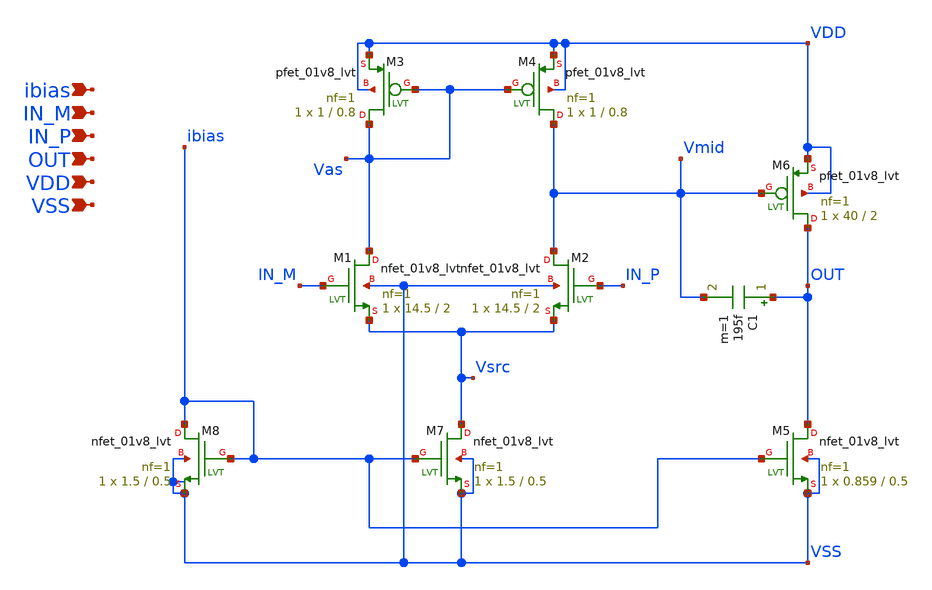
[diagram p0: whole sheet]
** sch_path: xchem/OTA3_kh.sch
**.subckt OTA3_kh IN_M IN_P OUT ibias VDD VSS
*.ipin IN_M
*.ipin IN_P
*.ipin OUT
*.ipin ibias
*.ipin VDD
*.ipin VSS
XM1 Vas IN_M Vsrc VSS sky130_fd_pr__nfet_01v8_lvt L=2 W=14.5 nf=1 ad='int((nf+1)/2) * W/nf * 0.29' as='int((nf+2)/2) * W/nf * 0.29'
+ pd='2*int((nf+1)/2) * (W/nf + 0.29)' ps='2*int((nf+2)/2) * (W/nf + 0.29)' nrd='0.29 / W' nrs='0.29 / W'
+ sa=0 sb=0 sd=0 mult=1 m=1
XM2 Vmid IN_P Vsrc VSS sky130_fd_pr__nfet_01v8_lvt L=2 W=14.5 nf=1 ad='int((nf+1)/2) * W/nf * 0.29' as='int((nf+2)/2) * W/nf * 0.29'
+ pd='2*int((nf+1)/2) * (W/nf + 0.29)' ps='2*int((nf+2)/2) * (W/nf + 0.29)' nrd='0.29 / W' nrs='0.29 / W'
+ sa=0 sb=0 sd=0 mult=1 m=1
XM3 Vas Vas VDD VDD sky130_fd_pr__pfet_01v8_lvt L=0.8 W=1 nf=1 ad='int((nf+1)/2) * W/nf * 0.29' as='int((nf+2)/2) * W/nf * 0.29'
+ pd='2*int((nf+1)/2) * (W/nf + 0.29)' ps='2*int((nf+2)/2) * (W/nf + 0.29)' nrd='0.29 / W' nrs='0.29 / W'
+ sa=0 sb=0 sd=0 mult=1 m=1
XM4 Vmid Vas VDD VDD sky130_fd_pr__pfet_01v8_lvt L=0.8 W=1 nf=1 ad='int((nf+1)/2) * W/nf * 0.29' as='int((nf+2)/2) * W/nf * 0.29'
+ pd='2*int((nf+1)/2) * (W/nf + 0.29)' ps='2*int((nf+2)/2) * (W/nf + 0.29)' nrd='0.29 / W' nrs='0.29 / W'
+ sa=0 sb=0 sd=0 mult=1 m=1
XM6 OUT Vmid VDD VDD sky130_fd_pr__pfet_01v8_lvt L=2 W=40 nf=1 ad='int((nf+1)/2) * W/nf * 0.29' as='int((nf+2)/2) * W/nf * 0.29'
+ pd='2*int((nf+1)/2) * (W/nf + 0.29)' ps='2*int((nf+2)/2) * (W/nf + 0.29)' nrd='0.29 / W' nrs='0.29 / W'
+ sa=0 sb=0 sd=0 mult=1 m=1
XM5 OUT ibias VSS VSS sky130_fd_pr__nfet_01v8_lvt L=0.5 W=0.859 nf=1 ad='int((nf+1)/2) * W/nf * 0.29'
+ as='int((nf+2)/2) * W/nf * 0.29' pd='2*int((nf+1)/2) * (W/nf + 0.29)' ps='2*int((nf+2)/2) * (W/nf + 0.29)'
+ nrd='0.29 / W' nrs='0.29 / W' sa=0 sb=0 sd=0 mult=1 m=1
XM7 Vsrc ibias VSS VSS sky130_fd_pr__nfet_01v8_lvt L=0.5 W=1.5 nf=1 ad='int((nf+1)/2) * W/nf * 0.29'
+ as='int((nf+2)/2) * W/nf * 0.29' pd='2*int((nf+1)/2) * (W/nf + 0.29)' ps='2*int((nf+2)/2) * (W/nf + 0.29)'
+ nrd='0.29 / W' nrs='0.29 / W' sa=0 sb=0 sd=0 mult=1 m=1
XM8 ibias ibias VSS VSS sky130_fd_pr__nfet_01v8_lvt L=0.5 W=1.5 nf=1 ad='int((nf+1)/2) * W/nf * 0.29'
+ as='int((nf+2)/2) * W/nf * 0.29' pd='2*int((nf+1)/2) * (W/nf + 0.29)' ps='2*int((nf+2)/2) * (W/nf + 0.29)'
+ nrd='0.29 / W' nrs='0.29 / W' sa=0 sb=0 sd=0 mult=1 m=1
C1 OUT Vmid 195f m=1
**.ends
.end
